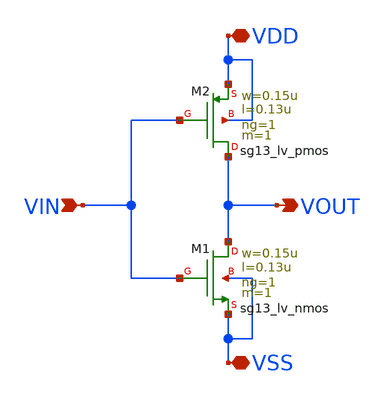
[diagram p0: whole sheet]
** sch_path: W2WDAC_Project/GROTDC/inv.sch
**.subckt inv VDD VSS VOUT VIN
*.iopin VDD
*.iopin VSS
*.opin VOUT
*.ipin VIN
XM2 VOUT VIN VDD VDD sg13_lv_pmos w=0.15u l=0.13u ng=1 m=1 mm_ok=1
XM1 VOUT VIN VSS VSS sg13_lv_nmos w=0.15u l=0.13u ng=1 m=1 mm_ok=1
**.ends
.end
